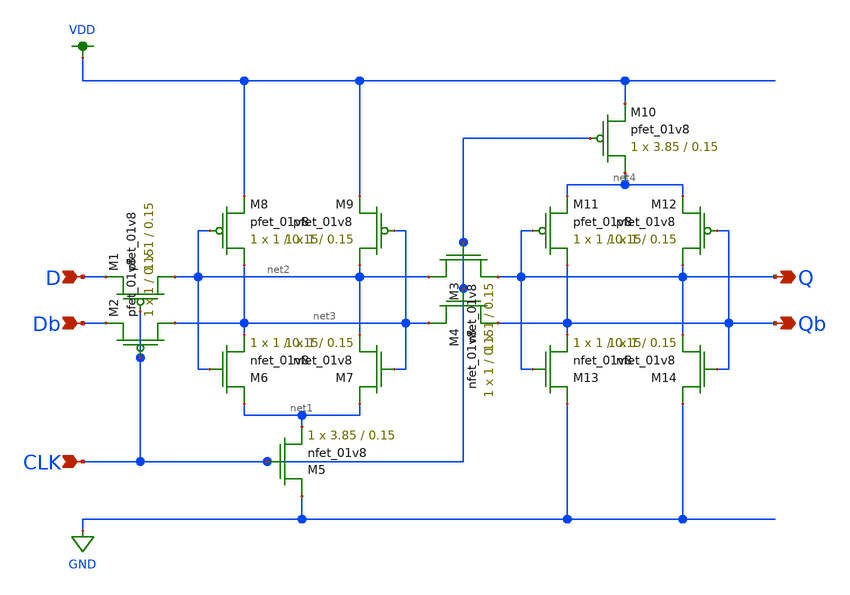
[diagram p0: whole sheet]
** sch_path: mp2/flipflop.sch
**.subckt flipflop D Db CLK Q Qb
*.ipin D
*.ipin Db
*.ipin CLK
*.opin Q
*.opin Qb
XM1 net2 CLK D VDD sky130_fd_pr__pfet_01v8 L=0.15 W=1 nf=1 ad='int((nf+1)/2) * W/nf * 0.29' as='int((nf+2)/2) * W/nf * 0.29'
+ pd='2*int((nf+1)/2) * (W/nf + 0.29)' ps='2*int((nf+2)/2) * (W/nf + 0.29)' nrd='0.29 / W' nrs='0.29 / W'
+ sa=0 sb=0 sd=0 mult=1 m=1
XM2 net3 CLK Db VDD sky130_fd_pr__pfet_01v8 L=0.15 W=1 nf=1 ad='int((nf+1)/2) * W/nf * 0.29' as='int((nf+2)/2) * W/nf * 0.29'
+ pd='2*int((nf+1)/2) * (W/nf + 0.29)' ps='2*int((nf+2)/2) * (W/nf + 0.29)' nrd='0.29 / W' nrs='0.29 / W'
+ sa=0 sb=0 sd=0 mult=1 m=1
XM3 net2 CLK Q GND sky130_fd_pr__nfet_01v8 L=0.15 W=1 nf=1 ad='int((nf+1)/2) * W/nf * 0.29' as='int((nf+2)/2) * W/nf * 0.29'
+ pd='2*int((nf+1)/2) * (W/nf + 0.29)' ps='2*int((nf+2)/2) * (W/nf + 0.29)' nrd='0.29 / W' nrs='0.29 / W'
+ sa=0 sb=0 sd=0 mult=1 m=1
XM4 net3 CLK Qb GND sky130_fd_pr__nfet_01v8 L=0.15 W=1 nf=1 ad='int((nf+1)/2) * W/nf * 0.29' as='int((nf+2)/2) * W/nf * 0.29'
+ pd='2*int((nf+1)/2) * (W/nf + 0.29)' ps='2*int((nf+2)/2) * (W/nf + 0.29)' nrd='0.29 / W' nrs='0.29 / W'
+ sa=0 sb=0 sd=0 mult=1 m=1
XM5 GND CLK net1 GND sky130_fd_pr__nfet_01v8 L=0.15 W=3.85 nf=1 ad='int((nf+1)/2) * W/nf * 0.29' as='int((nf+2)/2) * W/nf * 0.29'
+ pd='2*int((nf+1)/2) * (W/nf + 0.29)' ps='2*int((nf+2)/2) * (W/nf + 0.29)' nrd='0.29 / W' nrs='0.29 / W'
+ sa=0 sb=0 sd=0 mult=1 m=1
XM6 net1 net2 net3 GND sky130_fd_pr__nfet_01v8 L=0.15 W=1 nf=1 ad='int((nf+1)/2) * W/nf * 0.29' as='int((nf+2)/2) * W/nf * 0.29'
+ pd='2*int((nf+1)/2) * (W/nf + 0.29)' ps='2*int((nf+2)/2) * (W/nf + 0.29)' nrd='0.29 / W' nrs='0.29 / W'
+ sa=0 sb=0 sd=0 mult=1 m=1
XM7 net1 net3 net2 GND sky130_fd_pr__nfet_01v8 L=0.15 W=1 nf=1 ad='int((nf+1)/2) * W/nf * 0.29' as='int((nf+2)/2) * W/nf * 0.29'
+ pd='2*int((nf+1)/2) * (W/nf + 0.29)' ps='2*int((nf+2)/2) * (W/nf + 0.29)' nrd='0.29 / W' nrs='0.29 / W'
+ sa=0 sb=0 sd=0 mult=1 m=1
XM8 net3 net2 VDD VDD sky130_fd_pr__pfet_01v8 L=0.15 W=1 nf=1 ad='int((nf+1)/2) * W/nf * 0.29' as='int((nf+2)/2) * W/nf * 0.29'
+ pd='2*int((nf+1)/2) * (W/nf + 0.29)' ps='2*int((nf+2)/2) * (W/nf + 0.29)' nrd='0.29 / W' nrs='0.29 / W'
+ sa=0 sb=0 sd=0 mult=1 m=1
XM9 net2 net3 VDD VDD sky130_fd_pr__pfet_01v8 L=0.15 W=1 nf=1 ad='int((nf+1)/2) * W/nf * 0.29' as='int((nf+2)/2) * W/nf * 0.29'
+ pd='2*int((nf+1)/2) * (W/nf + 0.29)' ps='2*int((nf+2)/2) * (W/nf + 0.29)' nrd='0.29 / W' nrs='0.29 / W'
+ sa=0 sb=0 sd=0 mult=1 m=1
XM10 net4 CLK VDD VDD sky130_fd_pr__pfet_01v8 L=0.15 W=3.85 nf=1 ad='int((nf+1)/2) * W/nf * 0.29' as='int((nf+2)/2) * W/nf * 0.29'
+ pd='2*int((nf+1)/2) * (W/nf + 0.29)' ps='2*int((nf+2)/2) * (W/nf + 0.29)' nrd='0.29 / W' nrs='0.29 / W'
+ sa=0 sb=0 sd=0 mult=1 m=1
XM11 Qb Q net4 VDD sky130_fd_pr__pfet_01v8 L=0.15 W=1 nf=1 ad='int((nf+1)/2) * W/nf * 0.29' as='int((nf+2)/2) * W/nf * 0.29'
+ pd='2*int((nf+1)/2) * (W/nf + 0.29)' ps='2*int((nf+2)/2) * (W/nf + 0.29)' nrd='0.29 / W' nrs='0.29 / W'
+ sa=0 sb=0 sd=0 mult=1 m=1
XM12 Q Qb net4 VDD sky130_fd_pr__pfet_01v8 L=0.15 W=1 nf=1 ad='int((nf+1)/2) * W/nf * 0.29' as='int((nf+2)/2) * W/nf * 0.29'
+ pd='2*int((nf+1)/2) * (W/nf + 0.29)' ps='2*int((nf+2)/2) * (W/nf + 0.29)' nrd='0.29 / W' nrs='0.29 / W'
+ sa=0 sb=0 sd=0 mult=1 m=1
XM13 GND Q Qb GND sky130_fd_pr__nfet_01v8 L=0.15 W=1 nf=1 ad='int((nf+1)/2) * W/nf * 0.29' as='int((nf+2)/2) * W/nf * 0.29'
+ pd='2*int((nf+1)/2) * (W/nf + 0.29)' ps='2*int((nf+2)/2) * (W/nf + 0.29)' nrd='0.29 / W' nrs='0.29 / W'
+ sa=0 sb=0 sd=0 mult=1 m=1
XM14 GND Qb Q GND sky130_fd_pr__nfet_01v8 L=0.15 W=1 nf=1 ad='int((nf+1)/2) * W/nf * 0.29' as='int((nf+2)/2) * W/nf * 0.29'
+ pd='2*int((nf+1)/2) * (W/nf + 0.29)' ps='2*int((nf+2)/2) * (W/nf + 0.29)' nrd='0.29 / W' nrs='0.29 / W'
+ sa=0 sb=0 sd=0 mult=1 m=1
**.ends
.GLOBAL GND
.GLOBAL VDD
.end
